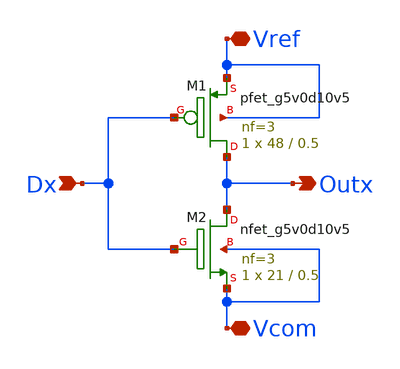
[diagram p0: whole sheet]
** sch_path: xschem/dac_switch.sch
**.subckt dac_switch Dx Outx Vref Vcom
*.ipin Dx
*.opin Outx
*.iopin Vref
*.iopin Vcom
XM1 Outx Dx Vref Vref sky130_fd_pr__pfet_g5v0d10v5 L=0.5 W=48 nf=3 ad='int((nf+1)/2) * W/nf * 0.29' as='int((nf+2)/2) * W/nf * 0.29'
+ pd='2*int((nf+1)/2) * (W/nf + 0.29)' ps='2*int((nf+2)/2) * (W/nf + 0.29)' nrd='0.29 / W' nrs='0.29 / W'
+ sa=0 sb=0 sd=0 mult=1 m=1
XM2 Outx Dx Vcom Vcom sky130_fd_pr__nfet_g5v0d10v5 L=0.5 W=21 nf=3 ad='int((nf+1)/2) * W/nf * 0.29' as='int((nf+2)/2) * W/nf * 0.29'
+ pd='2*int((nf+1)/2) * (W/nf + 0.29)' ps='2*int((nf+2)/2) * (W/nf + 0.29)' nrd='0.29 / W' nrs='0.29 / W'
+ sa=0 sb=0 sd=0 mult=1 m=1
**.ends
.end
